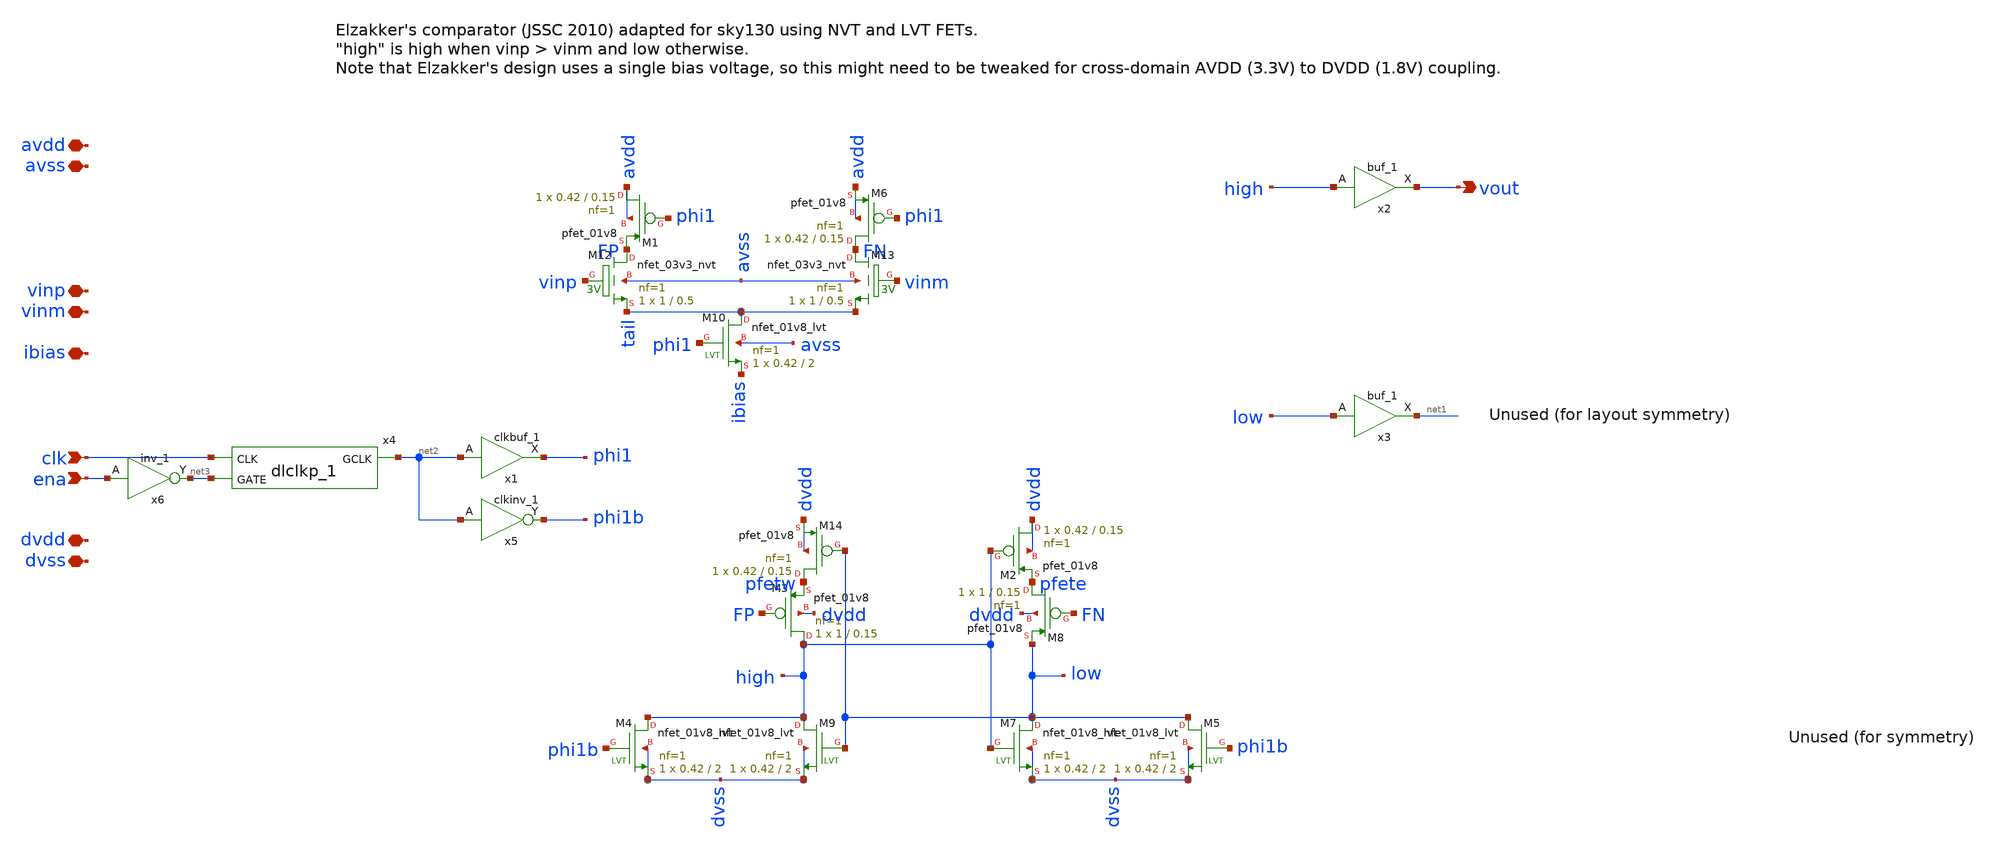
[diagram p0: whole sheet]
** sch_path: xschem/comparator_single_tail.sch
**.subckt comparator_single_tail clk vinp vinm dvdd dvss vout avdd avss ibias ena
*.ipin clk
*.iopin vinp
*.iopin vinm
*.iopin dvdd
*.iopin dvss
*.opin vout
*.iopin avdd
*.iopin avss
*.iopin ibias
*.ipin ena
XM12 FP vinp tail avss sky130_fd_pr__nfet_03v3_nvt L=0.5 W=1 nf=1 ad='int((nf+1)/2) * W/nf * 0.29' as='int((nf+2)/2) * W/nf * 0.29'
+ pd='2*int((nf+1)/2) * (W/nf + 0.29)' ps='2*int((nf+2)/2) * (W/nf + 0.29)' nrd='0.29 / W' nrs='0.29 / W'
+ sa=0 sb=0 sd=0 mult=1 m=1
XM13 FN vinm tail avss sky130_fd_pr__nfet_03v3_nvt L=0.5 W=1 nf=1 ad='int((nf+1)/2) * W/nf * 0.29' as='int((nf+2)/2) * W/nf * 0.29'
+ pd='2*int((nf+1)/2) * (W/nf + 0.29)' ps='2*int((nf+2)/2) * (W/nf + 0.29)' nrd='0.29 / W' nrs='0.29 / W'
+ sa=0 sb=0 sd=0 mult=1 m=1
XM14 pfetw low dvdd dvdd sky130_fd_pr__pfet_01v8 L=0.15 W=0.42 nf=1 ad='int((nf+1)/2) * W/nf * 0.29'
+ as='int((nf+2)/2) * W/nf * 0.29' pd='2*int((nf+1)/2) * (W/nf + 0.29)' ps='2*int((nf+2)/2) * (W/nf + 0.29)'
+ nrd='0.29 / W' nrs='0.29 / W' sa=0 sb=0 sd=0 mult=1 m=1
XM3 high FP pfetw dvdd sky130_fd_pr__pfet_01v8 L=0.15 W=1 nf=1 ad='int((nf+1)/2) * W/nf * 0.29' as='int((nf+2)/2) * W/nf * 0.29'
+ pd='2*int((nf+1)/2) * (W/nf + 0.29)' ps='2*int((nf+2)/2) * (W/nf + 0.29)' nrd='0.29 / W' nrs='0.29 / W'
+ sa=0 sb=0 sd=0 mult=1 m=1
XM8 pfete FN low dvdd sky130_fd_pr__pfet_01v8 L=0.15 W=1 nf=1 ad='int((nf+1)/2) * W/nf * 0.29' as='int((nf+2)/2) * W/nf * 0.29'
+ pd='2*int((nf+1)/2) * (W/nf + 0.29)' ps='2*int((nf+2)/2) * (W/nf + 0.29)' nrd='0.29 / W' nrs='0.29 / W'
+ sa=0 sb=0 sd=0 mult=1 m=1
XM2 dvdd high pfete dvdd sky130_fd_pr__pfet_01v8 L=0.15 W=0.42 nf=1 ad='int((nf+1)/2) * W/nf * 0.29'
+ as='int((nf+2)/2) * W/nf * 0.29' pd='2*int((nf+1)/2) * (W/nf + 0.29)' ps='2*int((nf+2)/2) * (W/nf + 0.29)'
+ nrd='0.29 / W' nrs='0.29 / W' sa=0 sb=0 sd=0 mult=1 m=1
XM7 low high dvss dvss sky130_fd_pr__nfet_01v8_lvt L=2 W=0.42 nf=1 ad='int((nf+1)/2) * W/nf * 0.29' as='int((nf+2)/2) * W/nf * 0.29'
+ pd='2*int((nf+1)/2) * (W/nf + 0.29)' ps='2*int((nf+2)/2) * (W/nf + 0.29)' nrd='0.29 / W' nrs='0.29 / W'
+ sa=0 sb=0 sd=0 mult=1 m=1
XM9 high low dvss dvss sky130_fd_pr__nfet_01v8_lvt L=2 W=0.42 nf=1 ad='int((nf+1)/2) * W/nf * 0.29' as='int((nf+2)/2) * W/nf * 0.29'
+ pd='2*int((nf+1)/2) * (W/nf + 0.29)' ps='2*int((nf+2)/2) * (W/nf + 0.29)' nrd='0.29 / W' nrs='0.29 / W'
+ sa=0 sb=0 sd=0 mult=1 m=1
XM10 tail phi1 ibias avss sky130_fd_pr__nfet_01v8_lvt L=2 W=0.42 nf=1 ad='int((nf+1)/2) * W/nf * 0.29'
+ as='int((nf+2)/2) * W/nf * 0.29' pd='2*int((nf+1)/2) * (W/nf + 0.29)' ps='2*int((nf+2)/2) * (W/nf + 0.29)'
+ nrd='0.29 / W' nrs='0.29 / W' sa=0 sb=0 sd=0 mult=1 m=1
XM1 avdd phi1 FP avdd sky130_fd_pr__pfet_01v8 L=0.15 W=0.42 nf=1 ad='int((nf+1)/2) * W/nf * 0.29' as='int((nf+2)/2) * W/nf * 0.29'
+ pd='2*int((nf+1)/2) * (W/nf + 0.29)' ps='2*int((nf+2)/2) * (W/nf + 0.29)' nrd='0.29 / W' nrs='0.29 / W'
+ sa=0 sb=0 sd=0 mult=1 m=1
XM6 FN phi1 avdd avdd sky130_fd_pr__pfet_01v8 L=0.15 W=0.42 nf=1 ad='int((nf+1)/2) * W/nf * 0.29' as='int((nf+2)/2) * W/nf * 0.29'
+ pd='2*int((nf+1)/2) * (W/nf + 0.29)' ps='2*int((nf+2)/2) * (W/nf + 0.29)' nrd='0.29 / W' nrs='0.29 / W'
+ sa=0 sb=0 sd=0 mult=1 m=1
XM4 high phi1b dvss dvss sky130_fd_pr__nfet_01v8_lvt L=2 W=0.42 nf=1 ad='int((nf+1)/2) * W/nf * 0.29'
+ as='int((nf+2)/2) * W/nf * 0.29' pd='2*int((nf+1)/2) * (W/nf + 0.29)' ps='2*int((nf+2)/2) * (W/nf + 0.29)'
+ nrd='0.29 / W' nrs='0.29 / W' sa=0 sb=0 sd=0 mult=1 m=1
XM5 low phi1b dvss dvss sky130_fd_pr__nfet_01v8_lvt L=2 W=0.42 nf=1 ad='int((nf+1)/2) * W/nf * 0.29'
+ as='int((nf+2)/2) * W/nf * 0.29' pd='2*int((nf+1)/2) * (W/nf + 0.29)' ps='2*int((nf+2)/2) * (W/nf + 0.29)'
+ nrd='0.29 / W' nrs='0.29 / W' sa=0 sb=0 sd=0 mult=1 m=1
x2 high dvss dvss dvdd dvdd vout sky130_fd_sc_hd__buf_1
x3 low dvss dvss dvdd dvdd net1 sky130_fd_sc_hd__buf_1
x4 clk net3 dvss dvss dvdd dvdd net2 sky130_fd_sc_hd__dlclkp_1
x1 net2 dvss dvss dvdd dvdd phi1 sky130_fd_sc_hd__clkbuf_1
x5 net2 dvss dvss dvdd dvdd phi1b sky130_fd_sc_hd__clkinv_1
x6 ena dvss dvss dvdd dvdd net3 sky130_fd_sc_hd__inv_1
**.ends
.end
